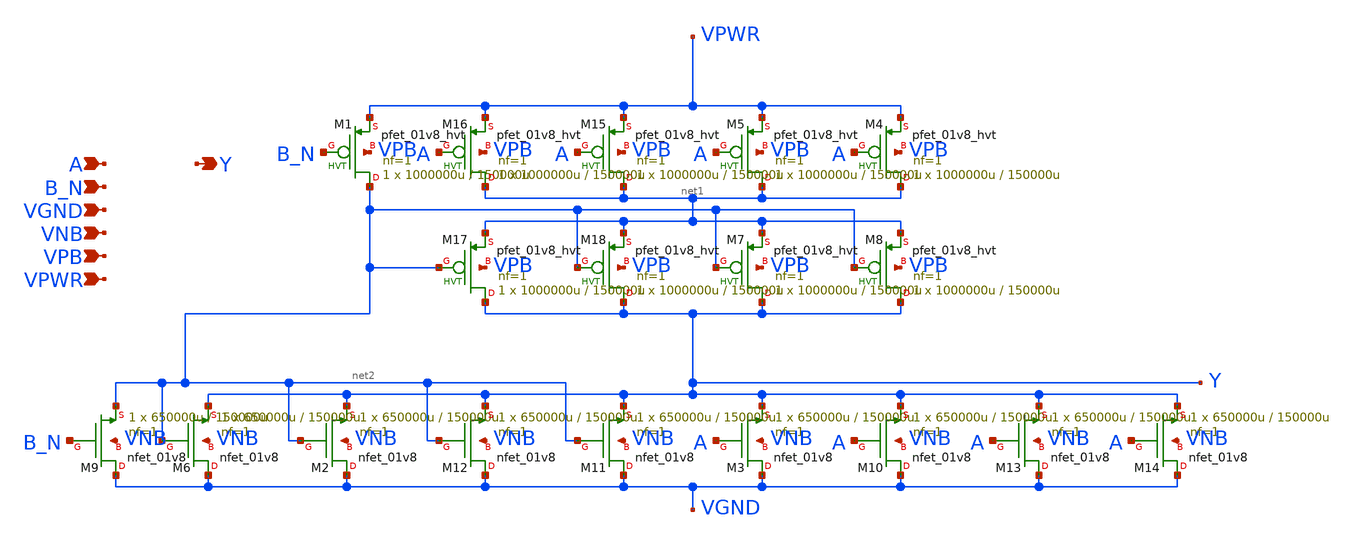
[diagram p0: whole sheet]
** sch_path: schematics/nor2b/sky130_fd_sc_hd__nor2b_4.sch
**.subckt sky130_fd_sc_hd__nor2b_4 A B_N VGND VNB VPB VPWR Y
*.ipin A
*.ipin B_N
*.ipin VGND
*.ipin VNB
*.ipin VPB
*.ipin VPWR
*.opin Y
XM1 net2 B_N VPWR VPB sky130_fd_pr__pfet_01v8_hvt L=150000u W=1000000u nf=1 ad='int((1 + 1)/2) * 1000000u / 1 * 0.29'
+ as='int((1 + 2)/2) * 1000000u / 1 * 0.29' pd='2*int((1 + 1)/2) * (1000000u / 1 + 0.29)' ps='2*int((1 + 2)/2) * (1000000u / 1 + 0.29)'
+ nrd='0.29 / 1000000u ' nrs='0.29 / 1000000u ' sa=0 sb=0 sd=0 mult=1 m=1
XM2 VGND net2 Y VNB sky130_fd_pr__nfet_01v8 L=150000u W=650000u nf=1 ad='int((1 + 1)/2) * 650000u / 1 * 0.29'
+ as='int((1 + 2)/2) * 650000u / 1 * 0.29' pd='2*int((1 + 1)/2) * (650000u / 1 + 0.29)' ps='2*int((1 + 2)/2) * (650000u / 1 + 0.29)'
+ nrd='0.29 / 650000u ' nrs='0.29 / 650000u ' sa=0 sb=0 sd=0 mult=1 m=1
XM4 net1 A VPWR VPB sky130_fd_pr__pfet_01v8_hvt L=150000u W=1000000u nf=1 ad='int((1 + 1)/2) * 1000000u / 1 * 0.29'
+ as='int((1 + 2)/2) * 1000000u / 1 * 0.29' pd='2*int((1 + 1)/2) * (1000000u / 1 + 0.29)' ps='2*int((1 + 2)/2) * (1000000u / 1 + 0.29)'
+ nrd='0.29 / 1000000u ' nrs='0.29 / 1000000u ' sa=0 sb=0 sd=0 mult=1 m=1
XM6 VGND net2 Y VNB sky130_fd_pr__nfet_01v8 L=150000u W=650000u nf=1 ad='int((1 + 1)/2) * 650000u / 1 * 0.29'
+ as='int((1 + 2)/2) * 650000u / 1 * 0.29' pd='2*int((1 + 1)/2) * (650000u / 1 + 0.29)' ps='2*int((1 + 2)/2) * (650000u / 1 + 0.29)'
+ nrd='0.29 / 650000u ' nrs='0.29 / 650000u ' sa=0 sb=0 sd=0 mult=1 m=1
XM5 net1 A VPWR VPB sky130_fd_pr__pfet_01v8_hvt L=150000u W=1000000u nf=1 ad='int((1 + 1)/2) * 1000000u / 1 * 0.29'
+ as='int((1 + 2)/2) * 1000000u / 1 * 0.29' pd='2*int((1 + 1)/2) * (1000000u / 1 + 0.29)' ps='2*int((1 + 2)/2) * (1000000u / 1 + 0.29)'
+ nrd='0.29 / 1000000u ' nrs='0.29 / 1000000u ' sa=0 sb=0 sd=0 mult=1 m=1
XM7 Y net2 net1 VPB sky130_fd_pr__pfet_01v8_hvt L=150000u W=1000000u nf=1 ad='int((1 + 1)/2) * 1000000u / 1 * 0.29'
+ as='int((1 + 2)/2) * 1000000u / 1 * 0.29' pd='2*int((1 + 1)/2) * (1000000u / 1 + 0.29)' ps='2*int((1 + 2)/2) * (1000000u / 1 + 0.29)'
+ nrd='0.29 / 1000000u ' nrs='0.29 / 1000000u ' sa=0 sb=0 sd=0 mult=1 m=1
XM8 Y net2 net1 VPB sky130_fd_pr__pfet_01v8_hvt L=150000u W=1000000u nf=1 ad='int((1 + 1)/2) * 1000000u / 1 * 0.29'
+ as='int((1 + 2)/2) * 1000000u / 1 * 0.29' pd='2*int((1 + 1)/2) * (1000000u / 1 + 0.29)' ps='2*int((1 + 2)/2) * (1000000u / 1 + 0.29)'
+ nrd='0.29 / 1000000u ' nrs='0.29 / 1000000u ' sa=0 sb=0 sd=0 mult=1 m=1
XM9 VGND B_N net2 VNB sky130_fd_pr__nfet_01v8 L=150000u W=650000u nf=1 ad='int((1 + 1)/2) * 650000u / 1 * 0.29'
+ as='int((1 + 2)/2) * 650000u / 1 * 0.29' pd='2*int((1 + 1)/2) * (650000u / 1 + 0.29)' ps='2*int((1 + 2)/2) * (650000u / 1 + 0.29)'
+ nrd='0.29 / 650000u ' nrs='0.29 / 650000u ' sa=0 sb=0 sd=0 mult=1 m=1
XM3 VGND A Y VNB sky130_fd_pr__nfet_01v8 L=150000u W=650000u nf=1 ad='int((1 + 1)/2) * 650000u / 1 * 0.29'
+ as='int((1 + 2)/2) * 650000u / 1 * 0.29' pd='2*int((1 + 1)/2) * (650000u / 1 + 0.29)' ps='2*int((1 + 2)/2) * (650000u / 1 + 0.29)'
+ nrd='0.29 / 650000u ' nrs='0.29 / 650000u ' sa=0 sb=0 sd=0 mult=1 m=1
XM10 VGND A Y VNB sky130_fd_pr__nfet_01v8 L=150000u W=650000u nf=1 ad='int((1 + 1)/2) * 650000u / 1 * 0.29'
+ as='int((1 + 2)/2) * 650000u / 1 * 0.29' pd='2*int((1 + 1)/2) * (650000u / 1 + 0.29)' ps='2*int((1 + 2)/2) * (650000u / 1 + 0.29)'
+ nrd='0.29 / 650000u ' nrs='0.29 / 650000u ' sa=0 sb=0 sd=0 mult=1 m=1
XM11 VGND net2 Y VNB sky130_fd_pr__nfet_01v8 L=150000u W=650000u nf=1 ad='int((1 + 1)/2) * 650000u / 1 * 0.29'
+ as='int((1 + 2)/2) * 650000u / 1 * 0.29' pd='2*int((1 + 1)/2) * (650000u / 1 + 0.29)' ps='2*int((1 + 2)/2) * (650000u / 1 + 0.29)'
+ nrd='0.29 / 650000u ' nrs='0.29 / 650000u ' sa=0 sb=0 sd=0 mult=1 m=1
XM12 VGND net2 Y VNB sky130_fd_pr__nfet_01v8 L=150000u W=650000u nf=1 ad='int((1 + 1)/2) * 650000u / 1 * 0.29'
+ as='int((1 + 2)/2) * 650000u / 1 * 0.29' pd='2*int((1 + 1)/2) * (650000u / 1 + 0.29)' ps='2*int((1 + 2)/2) * (650000u / 1 + 0.29)'
+ nrd='0.29 / 650000u ' nrs='0.29 / 650000u ' sa=0 sb=0 sd=0 mult=1 m=1
XM13 VGND A Y VNB sky130_fd_pr__nfet_01v8 L=150000u W=650000u nf=1 ad='int((1 + 1)/2) * 650000u / 1 * 0.29'
+ as='int((1 + 2)/2) * 650000u / 1 * 0.29' pd='2*int((1 + 1)/2) * (650000u / 1 + 0.29)' ps='2*int((1 + 2)/2) * (650000u / 1 + 0.29)'
+ nrd='0.29 / 650000u ' nrs='0.29 / 650000u ' sa=0 sb=0 sd=0 mult=1 m=1
XM14 VGND A Y VNB sky130_fd_pr__nfet_01v8 L=150000u W=650000u nf=1 ad='int((1 + 1)/2) * 650000u / 1 * 0.29'
+ as='int((1 + 2)/2) * 650000u / 1 * 0.29' pd='2*int((1 + 1)/2) * (650000u / 1 + 0.29)' ps='2*int((1 + 2)/2) * (650000u / 1 + 0.29)'
+ nrd='0.29 / 650000u ' nrs='0.29 / 650000u ' sa=0 sb=0 sd=0 mult=1 m=1
XM15 net1 A VPWR VPB sky130_fd_pr__pfet_01v8_hvt L=150000u W=1000000u nf=1 ad='int((1 + 1)/2) * 1000000u / 1 * 0.29'
+ as='int((1 + 2)/2) * 1000000u / 1 * 0.29' pd='2*int((1 + 1)/2) * (1000000u / 1 + 0.29)' ps='2*int((1 + 2)/2) * (1000000u / 1 + 0.29)'
+ nrd='0.29 / 1000000u ' nrs='0.29 / 1000000u ' sa=0 sb=0 sd=0 mult=1 m=1
XM16 net1 A VPWR VPB sky130_fd_pr__pfet_01v8_hvt L=150000u W=1000000u nf=1 ad='int((1 + 1)/2) * 1000000u / 1 * 0.29'
+ as='int((1 + 2)/2) * 1000000u / 1 * 0.29' pd='2*int((1 + 1)/2) * (1000000u / 1 + 0.29)' ps='2*int((1 + 2)/2) * (1000000u / 1 + 0.29)'
+ nrd='0.29 / 1000000u ' nrs='0.29 / 1000000u ' sa=0 sb=0 sd=0 mult=1 m=1
XM17 Y net2 net1 VPB sky130_fd_pr__pfet_01v8_hvt L=150000u W=1000000u nf=1 ad='int((1 + 1)/2) * 1000000u / 1 * 0.29'
+ as='int((1 + 2)/2) * 1000000u / 1 * 0.29' pd='2*int((1 + 1)/2) * (1000000u / 1 + 0.29)' ps='2*int((1 + 2)/2) * (1000000u / 1 + 0.29)'
+ nrd='0.29 / 1000000u ' nrs='0.29 / 1000000u ' sa=0 sb=0 sd=0 mult=1 m=1
XM18 Y net2 net1 VPB sky130_fd_pr__pfet_01v8_hvt L=150000u W=1000000u nf=1 ad='int((1 + 1)/2) * 1000000u / 1 * 0.29'
+ as='int((1 + 2)/2) * 1000000u / 1 * 0.29' pd='2*int((1 + 1)/2) * (1000000u / 1 + 0.29)' ps='2*int((1 + 2)/2) * (1000000u / 1 + 0.29)'
+ nrd='0.29 / 1000000u ' nrs='0.29 / 1000000u ' sa=0 sb=0 sd=0 mult=1 m=1
**.ends
.end
